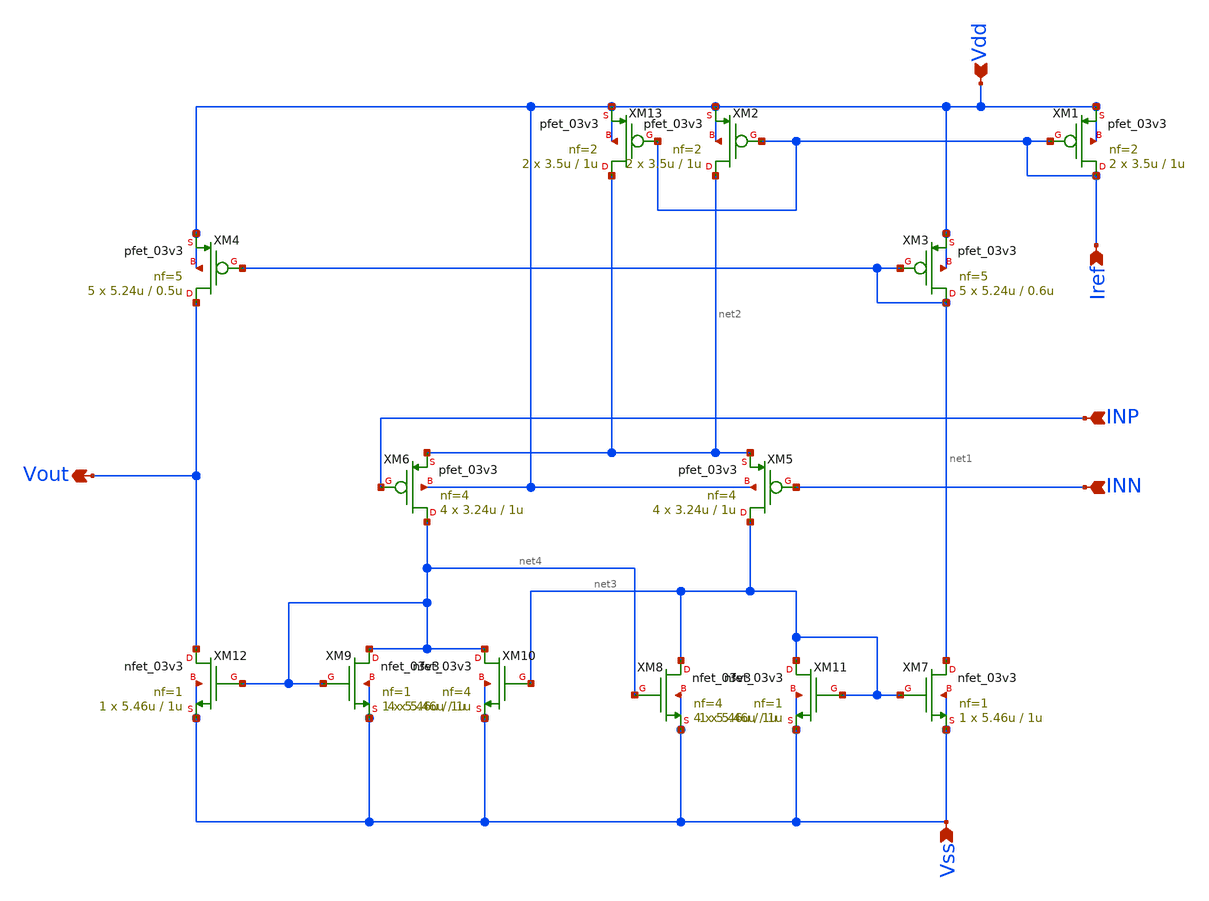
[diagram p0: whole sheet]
** sch_path: designs/libs/core_analog/Comparator/Pmos_Comparator.sch
**.subckt Pmos_Comparator Vdd Vss Iref INN INP Vout
*.ipin Vdd
*.ipin Vss
*.ipin Iref
*.ipin INN
*.ipin INP
*.opin Vout
XM1 Iref Iref Vdd Vdd pfet_03v3 L=1u W=3.5u nf=2 ad='int((nf+1)/2) * W/nf * 0.18u' as='int((nf+2)/2) * W/nf * 0.18u'
+ pd='2*int((nf+1)/2) * (W/nf + 0.18u)' ps='2*int((nf+2)/2) * (W/nf + 0.18u)' nrd='0.18u / W' nrs='0.18u / W'
+ sa=0 sb=0 sd=0 m=2
XM2 net2 Iref Vdd Vdd pfet_03v3 L=1u W=3.5u nf=2 ad='int((nf+1)/2) * W/nf * 0.18u' as='int((nf+2)/2) * W/nf * 0.18u'
+ pd='2*int((nf+1)/2) * (W/nf + 0.18u)' ps='2*int((nf+2)/2) * (W/nf + 0.18u)' nrd='0.18u / W' nrs='0.18u / W'
+ sa=0 sb=0 sd=0 m=2
XM3 net1 net1 Vdd Vdd pfet_03v3 L=0.6u W=5.24u nf=5 ad='int((nf+1)/2) * W/nf * 0.18u' as='int((nf+2)/2) * W/nf * 0.18u'
+ pd='2*int((nf+1)/2) * (W/nf + 0.18u)' ps='2*int((nf+2)/2) * (W/nf + 0.18u)' nrd='0.18u / W' nrs='0.18u / W'
+ sa=0 sb=0 sd=0 m=5
XM4 Vout net1 Vdd Vdd pfet_03v3 L=0.5u W=5.24u nf=5 ad='int((nf+1)/2) * W/nf * 0.18u' as='int((nf+2)/2) * W/nf * 0.18u'
+ pd='2*int((nf+1)/2) * (W/nf + 0.18u)' ps='2*int((nf+2)/2) * (W/nf + 0.18u)' nrd='0.18u / W' nrs='0.18u / W'
+ sa=0 sb=0 sd=0 m=5
XM5 net3 INN net2 Vdd pfet_03v3 L=1u W=3.24u nf=4 ad='int((nf+1)/2) * W/nf * 0.18u' as='int((nf+2)/2) * W/nf * 0.18u'
+ pd='2*int((nf+1)/2) * (W/nf + 0.18u)' ps='2*int((nf+2)/2) * (W/nf + 0.18u)' nrd='0.18u / W' nrs='0.18u / W'
+ sa=0 sb=0 sd=0 m=4
XM6 net4 INP net2 Vdd pfet_03v3 L=1u W=3.24u nf=4 ad='int((nf+1)/2) * W/nf * 0.18u' as='int((nf+2)/2) * W/nf * 0.18u'
+ pd='2*int((nf+1)/2) * (W/nf + 0.18u)' ps='2*int((nf+2)/2) * (W/nf + 0.18u)' nrd='0.18u / W' nrs='0.18u / W'
+ sa=0 sb=0 sd=0 m=4
XM7 net1 net3 Vss Vss nfet_03v3 L=1u W=5.46u nf=1 ad='int((nf+1)/2) * W/nf * 0.18u' as='int((nf+2)/2) * W/nf * 0.18u'
+ pd='2*int((nf+1)/2) * (W/nf + 0.18u)' ps='2*int((nf+2)/2) * (W/nf + 0.18u)' nrd='0.18u / W' nrs='0.18u / W'
+ sa=0 sb=0 sd=0 m=1
XM8 net3 net4 Vss Vss nfet_03v3 L=1u W=5.46u nf=4 ad='int((nf+1)/2) * W/nf * 0.18u' as='int((nf+2)/2) * W/nf * 0.18u'
+ pd='2*int((nf+1)/2) * (W/nf + 0.18u)' ps='2*int((nf+2)/2) * (W/nf + 0.18u)' nrd='0.18u / W' nrs='0.18u / W'
+ sa=0 sb=0 sd=0 m=4
XM9 net4 net4 Vss Vss nfet_03v3 L=1u W=5.46u nf=1 ad='int((nf+1)/2) * W/nf * 0.18u' as='int((nf+2)/2) * W/nf * 0.18u'
+ pd='2*int((nf+1)/2) * (W/nf + 0.18u)' ps='2*int((nf+2)/2) * (W/nf + 0.18u)' nrd='0.18u / W' nrs='0.18u / W'
+ sa=0 sb=0 sd=0 m=1
XM10 net4 net3 Vss Vss nfet_03v3 L=1u W=5.46u nf=4 ad='int((nf+1)/2) * W/nf * 0.18u' as='int((nf+2)/2) * W/nf * 0.18u'
+ pd='2*int((nf+1)/2) * (W/nf + 0.18u)' ps='2*int((nf+2)/2) * (W/nf + 0.18u)' nrd='0.18u / W' nrs='0.18u / W'
+ sa=0 sb=0 sd=0 m=4
XM11 net3 net3 Vss Vss nfet_03v3 L=1u W=5.46u nf=1 ad='int((nf+1)/2) * W/nf * 0.18u' as='int((nf+2)/2) * W/nf * 0.18u'
+ pd='2*int((nf+1)/2) * (W/nf + 0.18u)' ps='2*int((nf+2)/2) * (W/nf + 0.18u)' nrd='0.18u / W' nrs='0.18u / W'
+ sa=0 sb=0 sd=0 m=1
XM12 Vout net4 Vss Vss nfet_03v3 L=1u W=5.46u nf=1 ad='int((nf+1)/2) * W/nf * 0.18u' as='int((nf+2)/2) * W/nf * 0.18u'
+ pd='2*int((nf+1)/2) * (W/nf + 0.18u)' ps='2*int((nf+2)/2) * (W/nf + 0.18u)' nrd='0.18u / W' nrs='0.18u / W'
+ sa=0 sb=0 sd=0 m=1
XM13 net2 Iref Vdd Vdd pfet_03v3 L=1u W=3.5u nf=2 ad='int((nf+1)/2) * W/nf * 0.18u' as='int((nf+2)/2) * W/nf * 0.18u'
+ pd='2*int((nf+1)/2) * (W/nf + 0.18u)' ps='2*int((nf+2)/2) * (W/nf + 0.18u)' nrd='0.18u / W' nrs='0.18u / W'
+ sa=0 sb=0 sd=0 m=2
**.ends
.end
